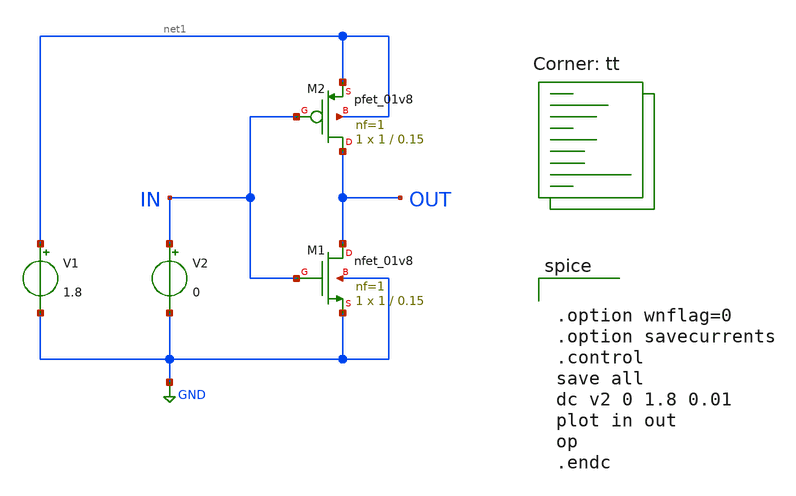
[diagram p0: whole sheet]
** sch_path: ring_oscillator/inverter_tb.sch
**.subckt inverter_tb
XM1 OUT IN GND GND sky130_fd_pr__nfet_01v8 L=0.15 W=1 nf=1 ad='int((nf+1)/2) * W/nf * 0.29' as='int((nf+2)/2) * W/nf * 0.29'
+ pd='2*int((nf+1)/2) * (W/nf + 0.29)' ps='2*int((nf+2)/2) * (W/nf + 0.29)' nrd='0.29 / W' nrs='0.29 / W'
+ sa=0 sb=0 sd=0 mult=1 m=1
XM2 OUT IN net1 net1 sky130_fd_pr__pfet_01v8 L=0.15 W=1 nf=1 ad='int((nf+1)/2) * W/nf * 0.29' as='int((nf+2)/2) * W/nf * 0.29'
+ pd='2*int((nf+1)/2) * (W/nf + 0.29)' ps='2*int((nf+2)/2) * (W/nf + 0.29)' nrd='0.29 / W' nrs='0.29 / W'
+ sa=0 sb=0 sd=0 mult=1 m=1
V1 net1 GND 1.8
V2 IN GND 0
**** begin user architecture code


.option wnflag=0
.option savecurrents
.control
save all
dc v2 0 1.8 0.01
plot in out
op
.endc


.lib $::SKYWATER_MODELS/sky130.lib.spice tt
**** end user architecture code
**.ends
.GLOBAL GND
.end
